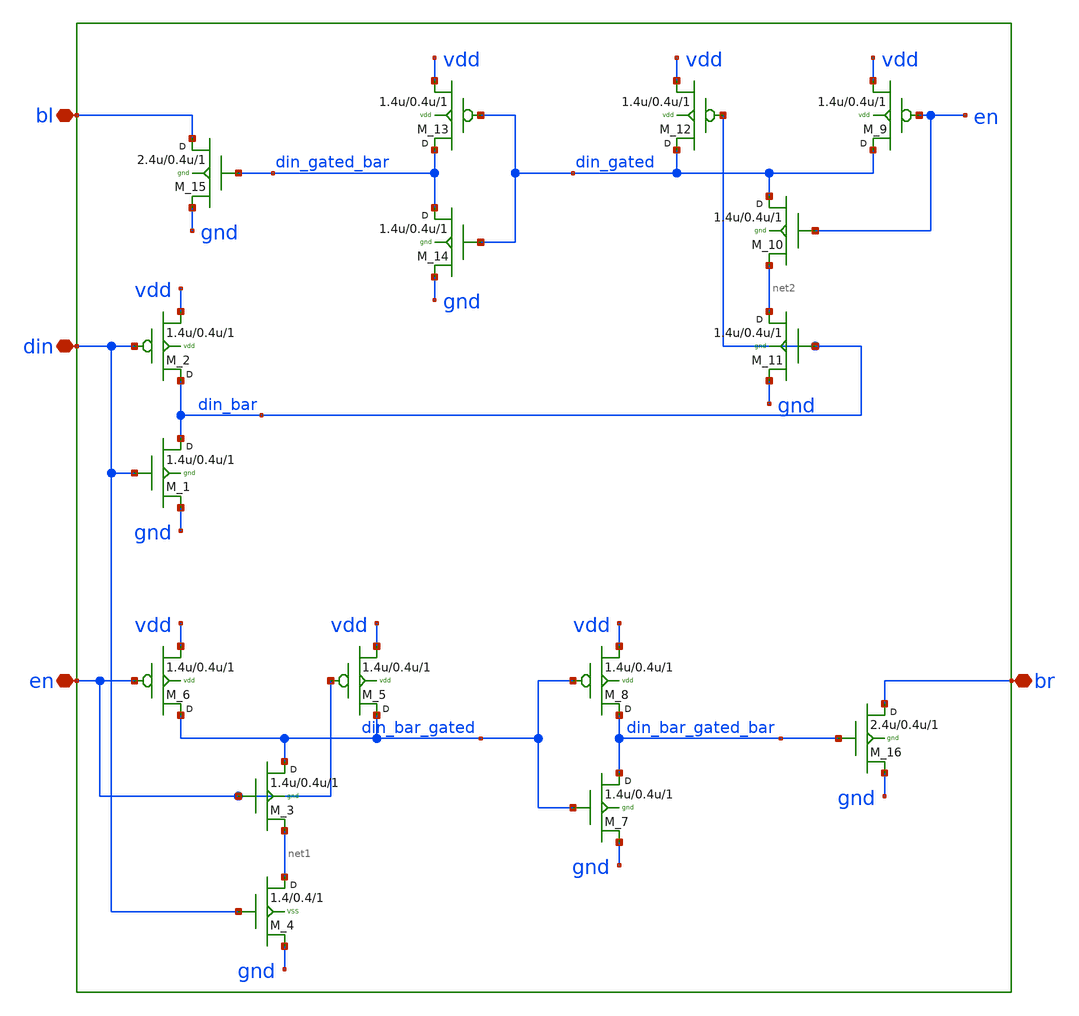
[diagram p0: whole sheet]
** sch_path: sram_2_16_scn4m/write_driver.sch
**.subckt write_driver din bl br en
*.iopin din
*.iopin bl
*.iopin br
*.iopin en
M_1 din_bar din gnd gnd n w=1.4u l=0.4u m=1
M_2 din_bar din vdd vdd p w=1.4u l=0.4u m=1
M_6 din_bar_gated en vdd vdd p w=1.4u l=0.4u m=1
M_5 din_bar_gated en vdd vdd p w=1.4u l=0.4u m=1
M_3 din_bar_gated en net1 gnd n w=1.4u l=0.4u m=1
M_4 net1 din gnd VSS nfet_01v8 w=1.4 l=0.4 m=1
M_7 din_bar_gated_bar din_bar_gated gnd gnd n w=1.4u l=0.4u m=1
M_8 din_bar_gated_bar din_bar_gated vdd vdd p w=1.4u l=0.4u m=1
M_9 din_gated en vdd vdd p w=1.4u l=0.4u m=1
M_12 din_gated din_bar vdd vdd p w=1.4u l=0.4u m=1
M_10 din_gated en net2 gnd n w=1.4u l=0.4u m=1
M_11 net2 din_bar gnd gnd n w=1.4u l=0.4u m=1
M_14 din_gated_bar din_gated gnd gnd n w=1.4u l=0.4u m=1
M_13 din_gated_bar din_gated vdd vdd p w=1.4u l=0.4u m=1
M_15 bl din_gated_bar gnd gnd n w=2.4u l=0.4u m=1
M_16 br din_bar_gated_bar gnd gnd n w=2.4u l=0.4u m=1
**.ends
.end
